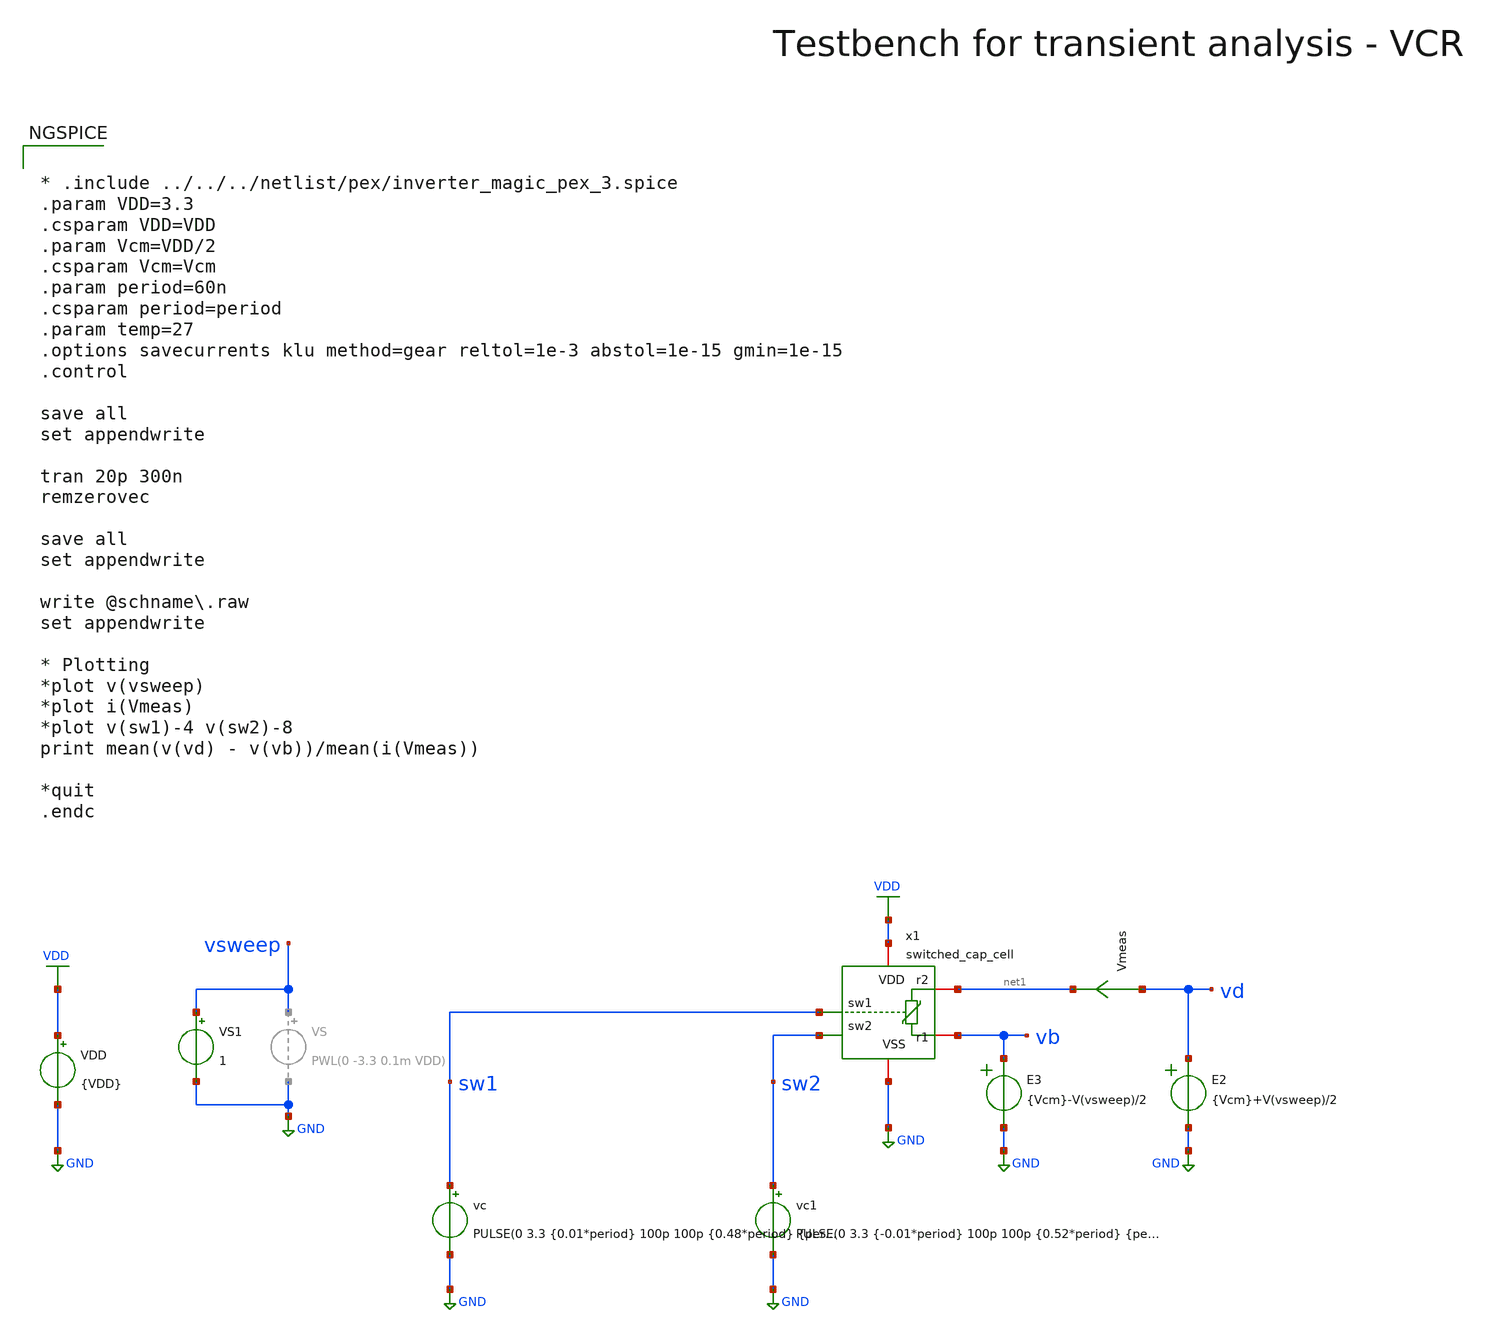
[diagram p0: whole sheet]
** sch_path: macros/heichips26_vcr/macros/switched_capacitor/testbenches/xschem/res_tb_tran.sch
**.subckt res_tb_tran
VDD VDD GND {VDD}
Vmeas vd net1 0
.save i(vmeas)
E2 vd GND VOL=' {Vcm}+V(vsweep)/2 '
E3 vb GND VOL=' {Vcm}-V(vsweep)/2 '
vc sw1 GND PULSE(0 3.3 {0.01*period} 100p 100p {0.48*period} {period})
x1 sw1 VDD GND net1 vb sw2 switched_cap_cell
VS1 vsweep GND 1
vc1 sw2 GND PULSE(0 3.3 {-0.01*period} 100p 100p {0.52*period} {period})
**** begin user architecture code


* .include ../../../netlist/pex/inverter_magic_pex_3.spice
.param VDD=3.3
.csparam VDD=VDD
.param Vcm=VDD/2
.csparam Vcm=Vcm
.param period=60n
.csparam period=period
.param temp=27
.options savecurrents klu method=gear reltol=1e-3 abstol=1e-15 gmin=1e-15
.control

save all
set appendwrite

tran 20p 300n
remzerovec

save all
set appendwrite

write @schname\.raw
set appendwrite

* Plotting
*plot v(vsweep)
*plot i(Vmeas)
*plot v(sw1)-4 v(sw2)-8
print mean(v(vd) - v(vb))/mean(i(Vmeas))

*quit
.endc



.lib cornerMOSlv.lib mos_tt
.lib cornerMOShv.lib mos_tt
.lib cornerRES.lib res_typ
.lib cornerDIO.lib dio_tt

.include $::PDK_ROOT/$::PDK/libs.ref/sg13cmos5l_stdcell/spice/sg13cmos5l_stdcell.spice

**** end user architecture code
**.ends
.GLOBAL GND
.GLOBAL VDD
.end
